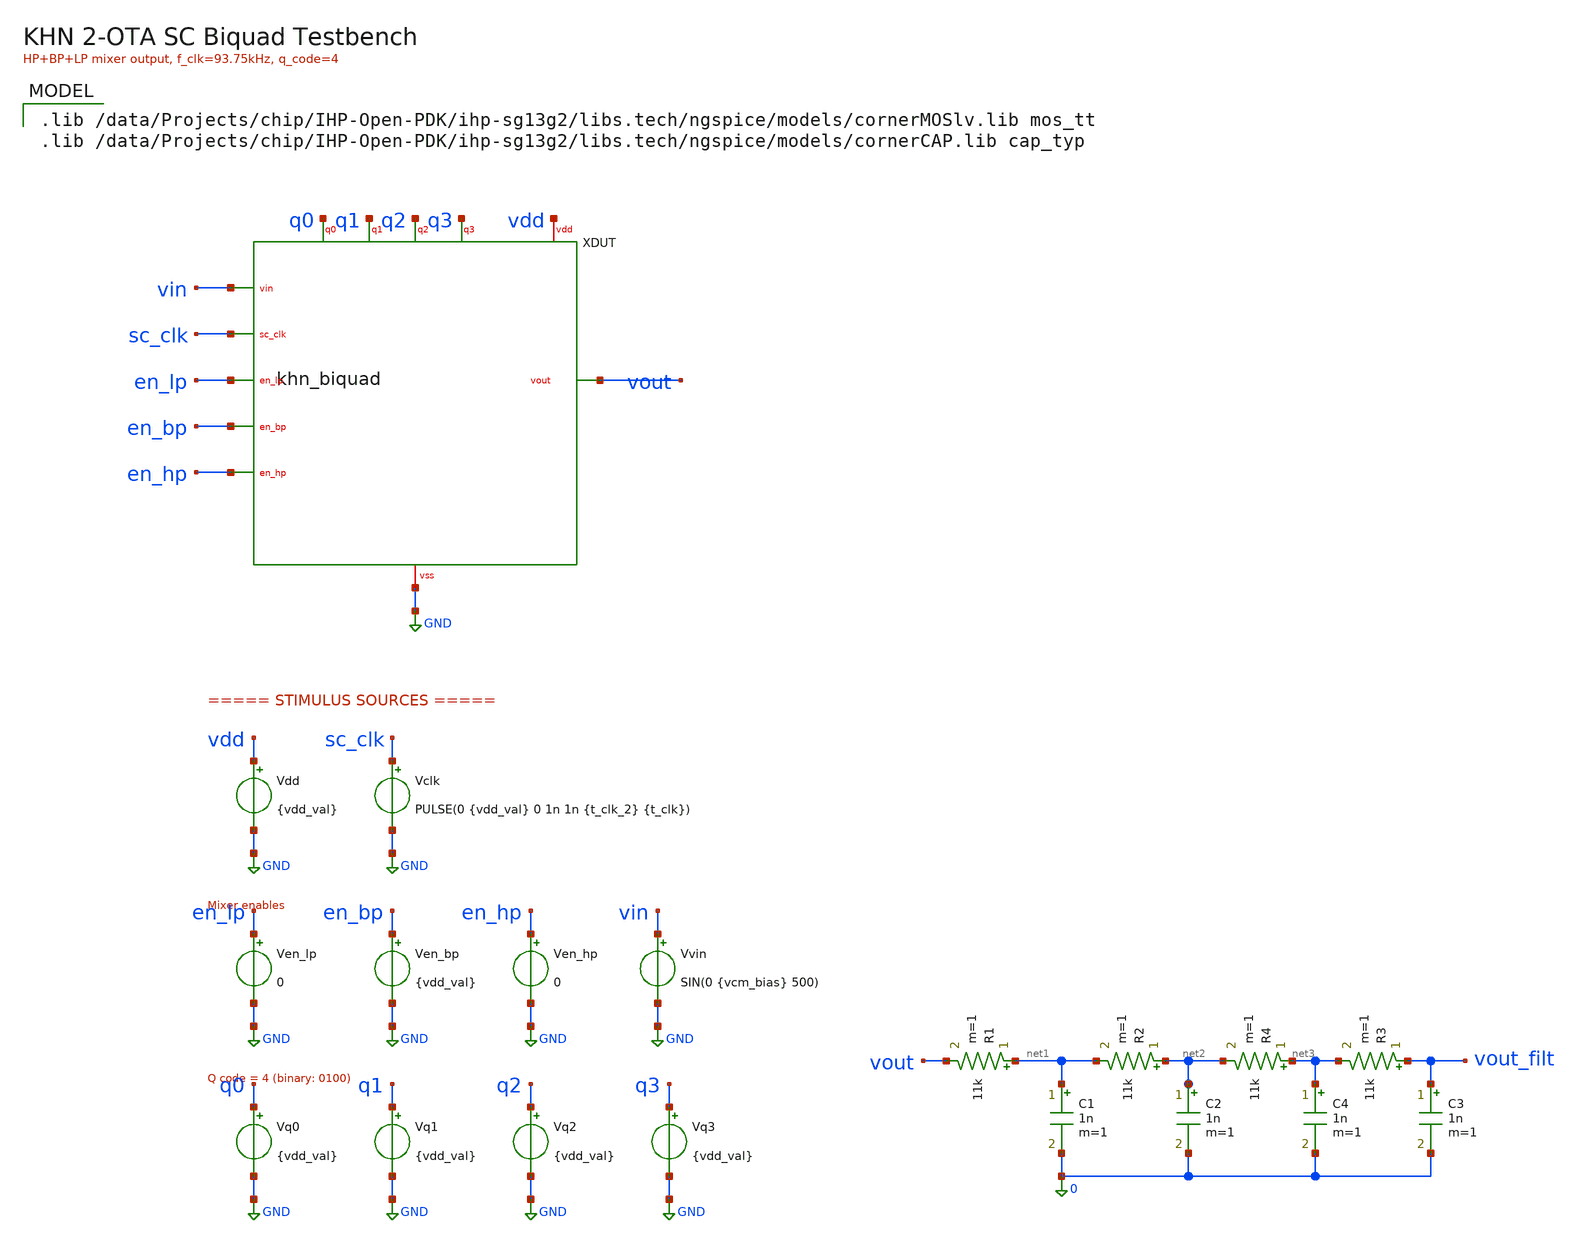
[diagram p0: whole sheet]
** sch_path: xschem/khn_biquad_tb.sch
**.subckt khn_biquad_tb
XDUT vin vout en_lp en_bp en_hp sc_clk q0 q1 q2 q3 vdd GND khn_biquad
Vdd vdd GND {vdd_val}
Vclk sc_clk GND PULSE(0 {vdd_val} 0 1n 1n {t_clk_2} {t_clk})
Vvin vin GND SIN(0 {vcm_bias} 500)
Ven_lp en_lp GND 0
Ven_bp en_bp GND {vdd_val}
Ven_hp en_hp GND 0
Vq0 q0 GND {vdd_val}
Vq1 q1 GND {vdd_val}
Vq2 q2 GND {vdd_val}
Vq3 q3 GND {vdd_val}
C1 net1 0 1n m=1
R1 net1 vout 11k m=1
R2 net2 net1 11k m=1
C2 net2 0 1n m=1
C3 vout_filt 0 1n m=1
R3 vout_filt net3 11k m=1
C4 net3 0 1n m=1
R4 net3 net2 11k m=1
**** begin user architecture code
 .lib /data/Projects/chip/IHP-Open-PDK/ihp-sg13g2/libs.tech/ngspice/models/cornerMOSlv.lib mos_tt
.lib /data/Projects/chip/IHP-Open-PDK/ihp-sg13g2/libs.tech/ngspice/models/cornerCAP.lib cap_typ



.options method=gear reltol=5e-3 abstol=1e-12 vntol=1e-6 gmin=1e-12
.param vdd_val = 1.2
.param f_clk = 13750
.param t_clk = {1/f_clk}
.param t_clk_2 = {t_clk/2 -1n}
.param vcm_bias = 0.47

* Force vcm to ideal voltage for SC debugging (bypasses weak bias gen)
Vvcm xdut.vcm 0 {vcm_bias}

* SC nodes float during DC OP — initialize near VCM and let transient settle
.ic v(xdut.bp)=0.614 v(xdut.lp)=0.614 v(xdut.hp)=0.47  v(xdut.sum1)=0.47 v(xdut.sum2)=0.47
+ v(xdut.sum3)=0.47  v(xdut.vcm)=0.47  v(xdut.cin_t)=0.47 v(xdut.cin_b)=0.47  v(xdut.cfb_t)=0.47 v(xdut.cfb_b)=0.47
+  v(xdut.cis_t)=0.47 v(xdut.cis_b)=0.47  v(xdut.c5_t)=0.47 v(xdut.c5_b)=0.47  v(xdut.c6_t)=0.47 v(xdut.c6_b)=0.47
+  v(xdut.cq0_t)=0.47 v(xdut.cq1_t)=0.47 v(xdut.cq2_t)=0.47 v(xdut.cq3_t)=0.47  v(xdut.x_ota1.mirr)=0.72
+ v(xdut.x_ota1.tail)=0.12  v(xdut.x_ota2.mirr)=0.72 v(xdut.x_ota2.tail)=0.12  v(xdut.x_ota3.mirr)=0.72
+ v(xdut.x_ota3.tail)=0.12  v(xdut.phi1)=0 v(xdut.n1)=1.2 v(xdut.n3)=1.2


.tran {t_clk/20} {800*t_clk} UIC
.control

  let start_freq = 10k
  let stop_freq = 260k
  let delta_freq = 50k
  let freq_act = start_freq

  * loop
  while freq_act le stop_freq
    *
    *reset
    *run
    let t_clk_new = {1/freq_act}
    let t_clk_2_new = {t_clk_new/2-1n}
    alterparam t_clk = $&t_clk_new
    alterparam t_clk_2 = $&t_clk_2_new

    print t_clk_2_new
    print t_clk_new

    *let f_clk = freq_act
    *let t_clk = {1/f_clk}
    *let t_clk_2 = {{t_clk/2}-1n}

    *print f_clk
    *print t_clk
    *print t_clk_2

    *alter @Vclk[PULSE] = [ 0 {vdd_val/2} 0 1n 1n $&t_clk_2 $&t_clk ]
    reset
    run
    write khn_biquad.out v(vout)
    write khn_biquad_tb.raw v(vin) v(vout) v(xdut.bp) v(xdut.lp) v(xdut.hp) v(xdut.sum1)
+ v(xdut.sum2) v(xdut.sum3)
    set wr_singlescale
    wrdata khn_biquad_tran.data v(vout) v(xdut.bp) v(xdut.lp) v(xdut.hp) v(xdut.vcm)
    let freq_act = freq_act + delta_freq


  end
  plot tran1.vout_filt tran2.vout_filt tran3.vout_filt tran4.vout_filt tran5.vout_filt
.endc


**** end user architecture code
**.ends

* expanding   symbol:  khn_biquad.sym # of pins=12
** sym_path: xschem/khn_biquad.sym
** sch_path: xschem/khn_biquad.sch
.subckt khn_biquad vin vout en_lp en_bp en_hp sc_clk q0 q1 q2 q3 vdd vss
*.ipin vin
*.opin vout
*.ipin en_lp
*.ipin en_bp
*.ipin en_hp
*.ipin sc_clk
*.ipin q0
*.ipin q1
*.ipin q2
*.ipin q3
*.iopin vdd
*.iopin vss
XXXMPbias vcm vcm vdd vdd sg13_lv_pmos w=2e-6 l=0.5e-6 ng=1 m=1 mm_ok=1
XXXMNbias vcm vcm vss vss sg13_lv_nmos w=2e-6 l=0.5e-6 ng=1 m=1 mm_ok=1
XXXMP_n0 n1 sc_clk vdd vdd sg13_lv_pmos w=2e-6 l=0.13e-6 ng=1 m=1 mm_ok=1
XXXMN_n0 n1 sc_clk vss vss sg13_lv_nmos w=1e-6 l=0.13e-6 ng=1 m=1 mm_ok=1
XXXMP_n1 phi1 n1 vdd vdd sg13_lv_pmos w=2e-6 l=0.13e-6 ng=1 m=1 mm_ok=1
XXXMN_n1 phi1 n1 vss vss sg13_lv_nmos w=1e-6 l=0.13e-6 ng=1 m=1 mm_ok=1
XXXMP_n2 n3 phi1 vdd vdd sg13_lv_pmos w=2e-6 l=0.13e-6 ng=1 m=1 mm_ok=1
XXXMN_n2 n3 phi1 vss vss sg13_lv_nmos w=1e-6 l=0.13e-6 ng=1 m=1 mm_ok=1
x_e1_top_vin vin cin_t phi1 n3 vss vdd cmos_tg
x_e1_bot_vcm vcm cin_b phi1 n3 vss vdd cmos_tg
x_e1_top_vcm vcm cin_t n3 phi1 vss vdd cmos_tg
x_e1_bot_sum sum1 cin_b n3 phi1 vss vdd cmos_tg
XXC_in cin_t cin_b cap_cmim w=7.0e-6 l=7.0e-6 m=1 mm_ok=1
x_e2_top_lp lp cfb_t phi1 n3 vss vdd cmos_tg
x_e2_bot_sum sum1 cfb_b phi1 n3 vss vdd cmos_tg
x_e2_top_vcm vcm cfb_t n3 phi1 vss vdd cmos_tg
x_e2_bot_vcm vcm cfb_b n3 phi1 vss vdd cmos_tg
XXC_fb cfb_t cfb_b cap_cmim w=7.0e-6 l=7.0e-6 m=1 mm_ok=1
XXC_int1 bp sum1 cap_cmim w=23.1e-6 l=23.1e-6 m=1 mm_ok=1
x_ota1 vcm sum1 vcm bp vdd vss svf_ota5t
x_e4_top_bp bp cis_t n3 phi1 vss vdd cmos_tg
x_e4_bot_vcm vcm cis_b n3 phi1 vss vdd cmos_tg
x_e4_top_vcm vcm cis_t phi1 n3 vss vdd cmos_tg
x_e4_bot_sum sum2 cis_b phi1 n3 vss vdd cmos_tg
XXC_is cis_t cis_b cap_cmim w=7.0e-6 l=7.0e-6 m=1 mm_ok=1
XXC_int2 lp sum2 cap_cmim w=23.1e-6 l=23.1e-6 m=1 mm_ok=1
x_ota2 vcm sum2 vcm lp vdd vss svf_ota5t
x_swq0_en bp net1 q0 q0_b vss vdd cmos_tg
x_swq0_phi net1 cq0_t phi1 n3 vss vdd cmos_tg
x_swq0_ref vcm cq0_t n3 phi1 vss vdd cmos_tg
XXC_q0 cq0_t sum1 cap_cmim w=1.81e-6 l=1.81e-6 m=1 mm_ok=1
x_swq1_en bp net2 q1 q1_b vss vdd cmos_tg
x_swq1_phi net2 cq1_t phi1 n3 vss vdd cmos_tg
x_swq1_ref vcm cq1_t n3 phi1 vss vdd cmos_tg
XXC_q1 cq1_t sum1 cap_cmim w=2.56e-6 l=2.56e-6 m=1 mm_ok=1
x_swq2_en bp net3 q2 q2_b vss vdd cmos_tg
x_swq2_phi net3 cq2_t phi1 n3 vss vdd cmos_tg
x_swq2_ref vcm cq2_t n3 phi1 vss vdd cmos_tg
XXC_q2 cq2_t sum1 cap_cmim w=3.62e-6 l=3.62e-6 m=1 mm_ok=1
x_swq3_en bp net4 q3 q3_b vss vdd cmos_tg
x_swq3_phi net4 cq3_t phi1 n3 vss vdd cmos_tg
x_swq3_ref vcm cq3_t n3 phi1 vss vdd cmos_tg
XXC_q3 cq3_t sum1 cap_cmim w=5.11e-6 l=5.11e-6 m=1 mm_ok=1
XXXMP_invq0 q0_b q0 vdd vdd sg13_lv_pmos w=2e-6 l=0.13e-6 ng=1 m=1 mm_ok=1
XXXMN_invq0 q0_b q0 vss vss sg13_lv_nmos w=1e-6 l=0.13e-6 ng=1 m=1 mm_ok=1
XXXMP_invq1 q1_b q1 vdd vdd sg13_lv_pmos w=2e-6 l=0.13e-6 ng=1 m=1 mm_ok=1
XXXMN_invq1 q1_b q1 vss vss sg13_lv_nmos w=1e-6 l=0.13e-6 ng=1 m=1 mm_ok=1
XXXMP_invq2 q2_b q2 vdd vdd sg13_lv_pmos w=2e-6 l=0.13e-6 ng=1 m=1 mm_ok=1
XXXMN_invq2 q2_b q2 vss vss sg13_lv_nmos w=1e-6 l=0.13e-6 ng=1 m=1 mm_ok=1
XXXMP_invq3 q3_b q3 vdd vdd sg13_lv_pmos w=2e-6 l=0.13e-6 ng=1 m=1 mm_ok=1
XXXMN_invq3 q3_b q3 vss vss sg13_lv_nmos w=1e-6 l=0.13e-6 ng=1 m=1 mm_ok=1
x_e5_top_vin vin c5_t phi1 n3 vss vdd cmos_tg
x_e5_bot_vcm vcm c5_b phi1 n3 vss vdd cmos_tg
x_e5_top_vcm vcm c5_t n3 phi1 vss vdd cmos_tg
x_e5_bot_sum3 sum3 c5_b n3 phi1 vss vdd cmos_tg
XXC5 c5_t c5_b cap_cmim w=7.0e-6 l=7.0e-6 m=1 mm_ok=1
x_e6_top_lp lp c6_t n3 phi1 vss vdd cmos_tg
x_e6_bot_sum3 sum3 c6_b n3 phi1 vss vdd cmos_tg
x_e6_top_vcm vcm c6_t phi1 n3 vss vdd cmos_tg
x_e6_bot_vcm vcm c6_b phi1 n3 vss vdd cmos_tg
XXC6 c6_t net5 cap_cmim w=7.0e-6 l=7.0e-6 m=1 mm_ok=1
x_hp_reset sum3 hp phi1 n3 vss vdd cmos_tg
XXC_hp hp sum3 cap_cmim w=7.0e-6 l=7.0e-6 m=1 mm_ok=1
x_ota3 vcm sum3 vcm hp vdd vss svf_ota5t
x_mix_lp lp vout en_lp en_lp_b vss vdd cmos_tg
x_mix_bp bp vout en_bp en_bp_b vss vdd cmos_tg
x_mix_hp hp vout en_hp en_hp_b vss vdd cmos_tg
XXXMP_inv_enlp en_lp_b en_lp vdd vdd sg13_lv_pmos w=2e-6 l=0.13e-6 ng=1 m=1 mm_ok=1
XXXMN_inv_enlp en_lp_b en_lp vss vss sg13_lv_nmos w=1e-6 l=0.13e-6 ng=1 m=1 mm_ok=1
XXXMP_inv_enbp en_bp_b en_bp vdd vdd sg13_lv_pmos w=2e-6 l=0.13e-6 ng=1 m=1 mm_ok=1
XXXMN_inv_enbp en_bp_b en_bp vss vss sg13_lv_nmos w=1e-6 l=0.13e-6 ng=1 m=1 mm_ok=1
XXXMP_inv_enhp en_hp_b en_hp vdd vdd sg13_lv_pmos w=2e-6 l=0.13e-6 ng=1 m=1 mm_ok=1
XXXMN_inv_enhp en_hp_b en_hp vss vss sg13_lv_nmos w=1e-6 l=0.13e-6 ng=1 m=1 mm_ok=1
.ends


* expanding   symbol:  cmos_tg.sym # of pins=6
** sym_path: xschem/cmos_tg.sym
** sch_path: xschem/cmos_tg.sch
.subckt cmos_tg a b ctrl_n ctrl_p vss vdd
*.iopin a
*.iopin b
*.ipin ctrl_p
*.iopin vss
*.iopin vdd
*.ipin ctrl_n
XXMN a ctrl_n b vss sg13_lv_nmos w=2e-6 l=0.13e-6 ng=1 m=1 mm_ok=1
XXMP b ctrl_p a vdd sg13_lv_pmos w=4e-6 l=0.13e-6 ng=1 m=1 mm_ok=1
.ends


* expanding   symbol:  svf_ota5t.sym # of pins=6
** sym_path: xschem/svf_ota5t.sym
** sch_path: xschem/svf_ota5t.sch
.subckt svf_ota5t vinp vinn vbias vout vdd vss
*.iopin vdd
*.iopin vss
*.ipin vinp
*.ipin vinn
*.opin vout
*.ipin vbias
XXM3 mirr mirr vdd vdd sg13_lv_pmos w=2e-6 l=0.5e-6 ng=1 m=1 mm_ok=1
XXM4 vout mirr vdd vdd sg13_lv_pmos w=2e-6 l=0.5e-6 ng=1 m=1 mm_ok=1
XXM1 mirr vinp tail vss sg13_lv_nmos w=4e-6 l=0.5e-6 ng=1 m=1 mm_ok=1
XXM2 vout vinn tail vss sg13_lv_nmos w=4e-6 l=0.5e-6 ng=1 m=1 mm_ok=1
XXM5 tail vbias vss vss sg13_lv_nmos w=2e-6 l=0.5e-6 ng=1 m=1 mm_ok=1
.ends

.GLOBAL GND
.end
